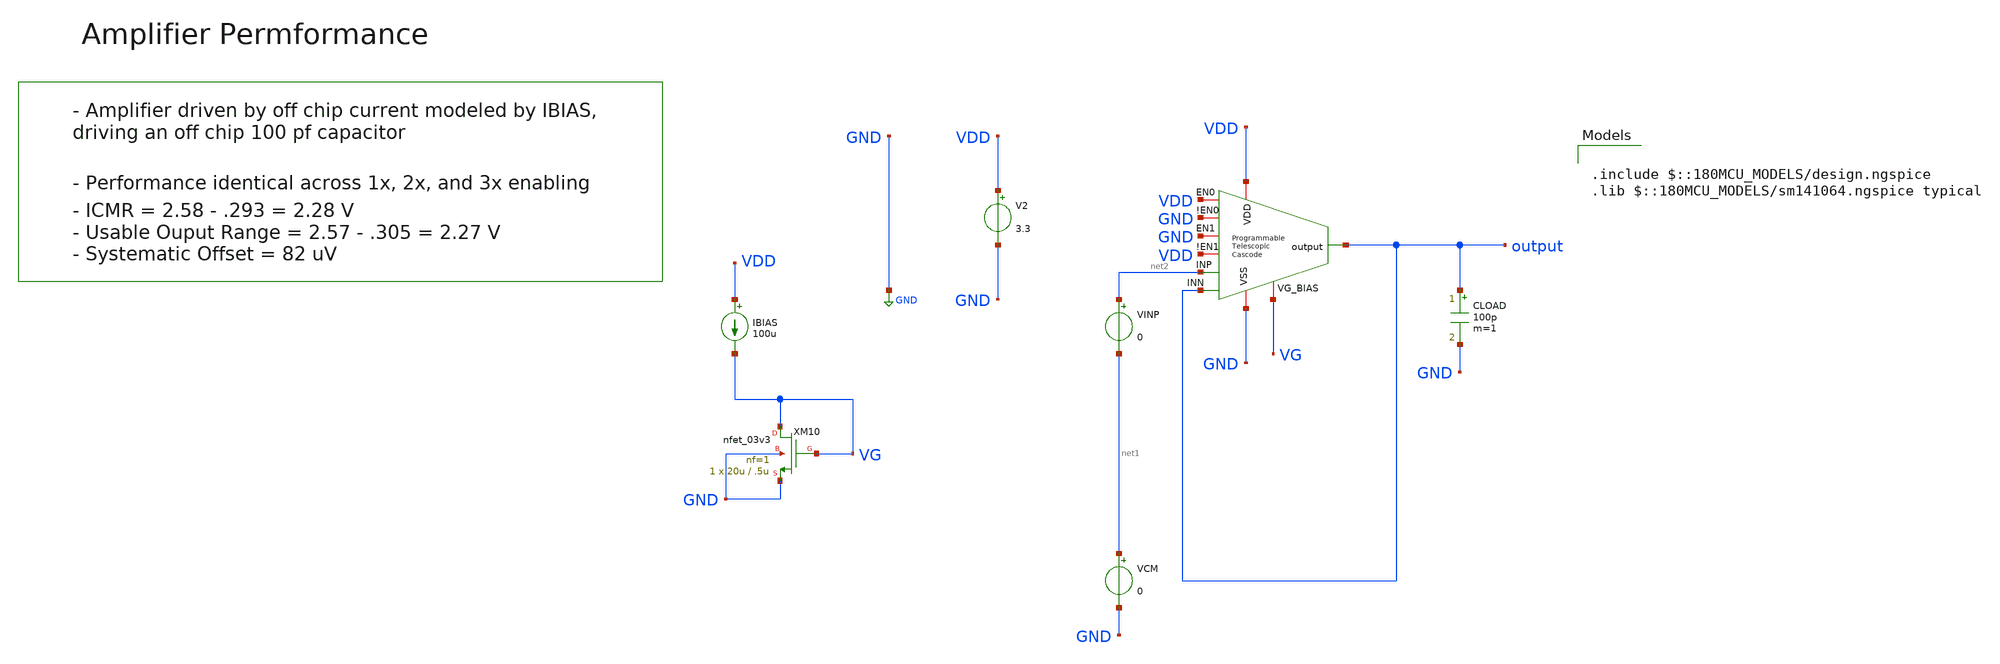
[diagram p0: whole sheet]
** sch_path: designs/libs/core_amps/ota_telescopic/programmable_tb/programmable_telescopic_cascode_dc_unity.sch
**.subckt programmable_telescopic_cascode_dc_unity
V2 VDD GND 3.3
CLOAD output GND 100p m=1
VINP net2 net1 0
VCM net1 GND 0
IBIAS VDD VG 100u
XM10 VG VG GND GND nfet_03v3 L=.5u W=20u nf=1 ad='int((nf+1)/2) * W/nf * 0.18u' as='int((nf+2)/2) * W/nf * 0.18u'
+ pd='2*int((nf+1)/2) * (W/nf + 0.18u)' ps='2*int((nf+2)/2) * (W/nf + 0.18u)' nrd='0.18u / W' nrs='0.18u / W'
+ sa=0 sb=0 sd=0 m=1
x1 VDD output VDD GND GND VDD output net2 GND VG programmable_telescopic_cascode
**** begin user architecture code

.include $::180MCU_MODELS/design.ngspice
.lib $::180MCU_MODELS/sm141064.ngspice typical



.control

dc VINP 0 4 0.001
let gain = deriv(v(output))
meas dc icmr_low when gain = 0.95 rise = 1
meas dc icmr_high when gain=0.95 fall=1 from=2
meas dc out_swing_high when gain=0.95 fall=1 from=2


print icmr_low icmr_high
print icmr_high - icmr_low
meas dc out_swing_low find v(output) when gain = 0.95 rise = 1
print out_swing_low out_swing_high
print out_swing_high - out_swing_low
plot v(output) gain
meas dc vos find v(output) at=1.65
let offset = vos - 1.65
print offset

.endc


**** end user architecture code
**.ends
.GLOBAL GND
.end
